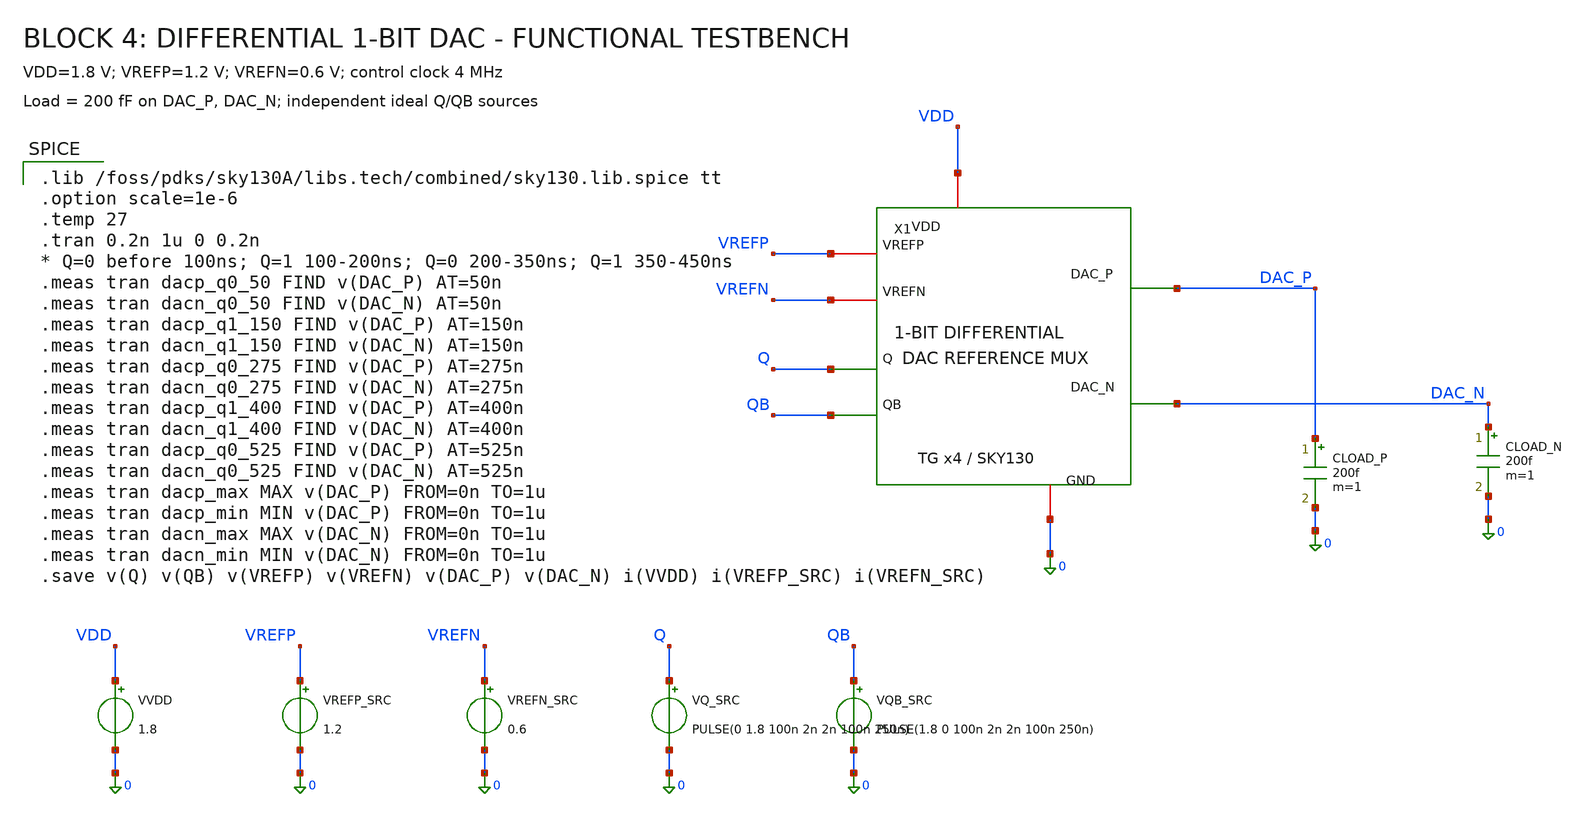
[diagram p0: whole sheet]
** sch_path: blocks/04_1Bit_DAC/sim/tb_DAC_1bit.sch
**.subckt tb_DAC_1bit
CLOAD_P DAC_P 0 200f m=1
CLOAD_N DAC_N 0 200f m=1
VVDD VDD 0 1.8
VREFP_SRC VREFP 0 1.2
VREFN_SRC VREFN 0 0.6
VQ_SRC Q 0 PULSE(0 1.8 100n 2n 2n 100n 250n)
VQB_SRC QB 0 PULSE(1.8 0 100n 2n 2n 100n 250n)
X1 VREFP VREFN Q QB VDD 0 DAC_P DAC_N DAC_1bit
**** begin user architecture code

.lib /foss/pdks/sky130A/libs.tech/combined/sky130.lib.spice tt
.option scale=1e-6
.temp 27
.tran 0.2n 1u 0 0.2n
* Q=0 before 100ns; Q=1 100-200ns; Q=0 200-350ns; Q=1 350-450ns
.meas tran dacp_q0_50 FIND v(DAC_P) AT=50n
.meas tran dacn_q0_50 FIND v(DAC_N) AT=50n
.meas tran dacp_q1_150 FIND v(DAC_P) AT=150n
.meas tran dacn_q1_150 FIND v(DAC_N) AT=150n
.meas tran dacp_q0_275 FIND v(DAC_P) AT=275n
.meas tran dacn_q0_275 FIND v(DAC_N) AT=275n
.meas tran dacp_q1_400 FIND v(DAC_P) AT=400n
.meas tran dacn_q1_400 FIND v(DAC_N) AT=400n
.meas tran dacp_q0_525 FIND v(DAC_P) AT=525n
.meas tran dacn_q0_525 FIND v(DAC_N) AT=525n
.meas tran dacp_max MAX v(DAC_P) FROM=0n TO=1u
.meas tran dacp_min MIN v(DAC_P) FROM=0n TO=1u
.meas tran dacn_max MAX v(DAC_N) FROM=0n TO=1u
.meas tran dacn_min MIN v(DAC_N) FROM=0n TO=1u
.save v(Q) v(QB) v(VREFP) v(VREFN) v(DAC_P) v(DAC_N) i(VVDD) i(VREFP_SRC) i(VREFN_SRC)

**** end user architecture code
**.ends
.end
